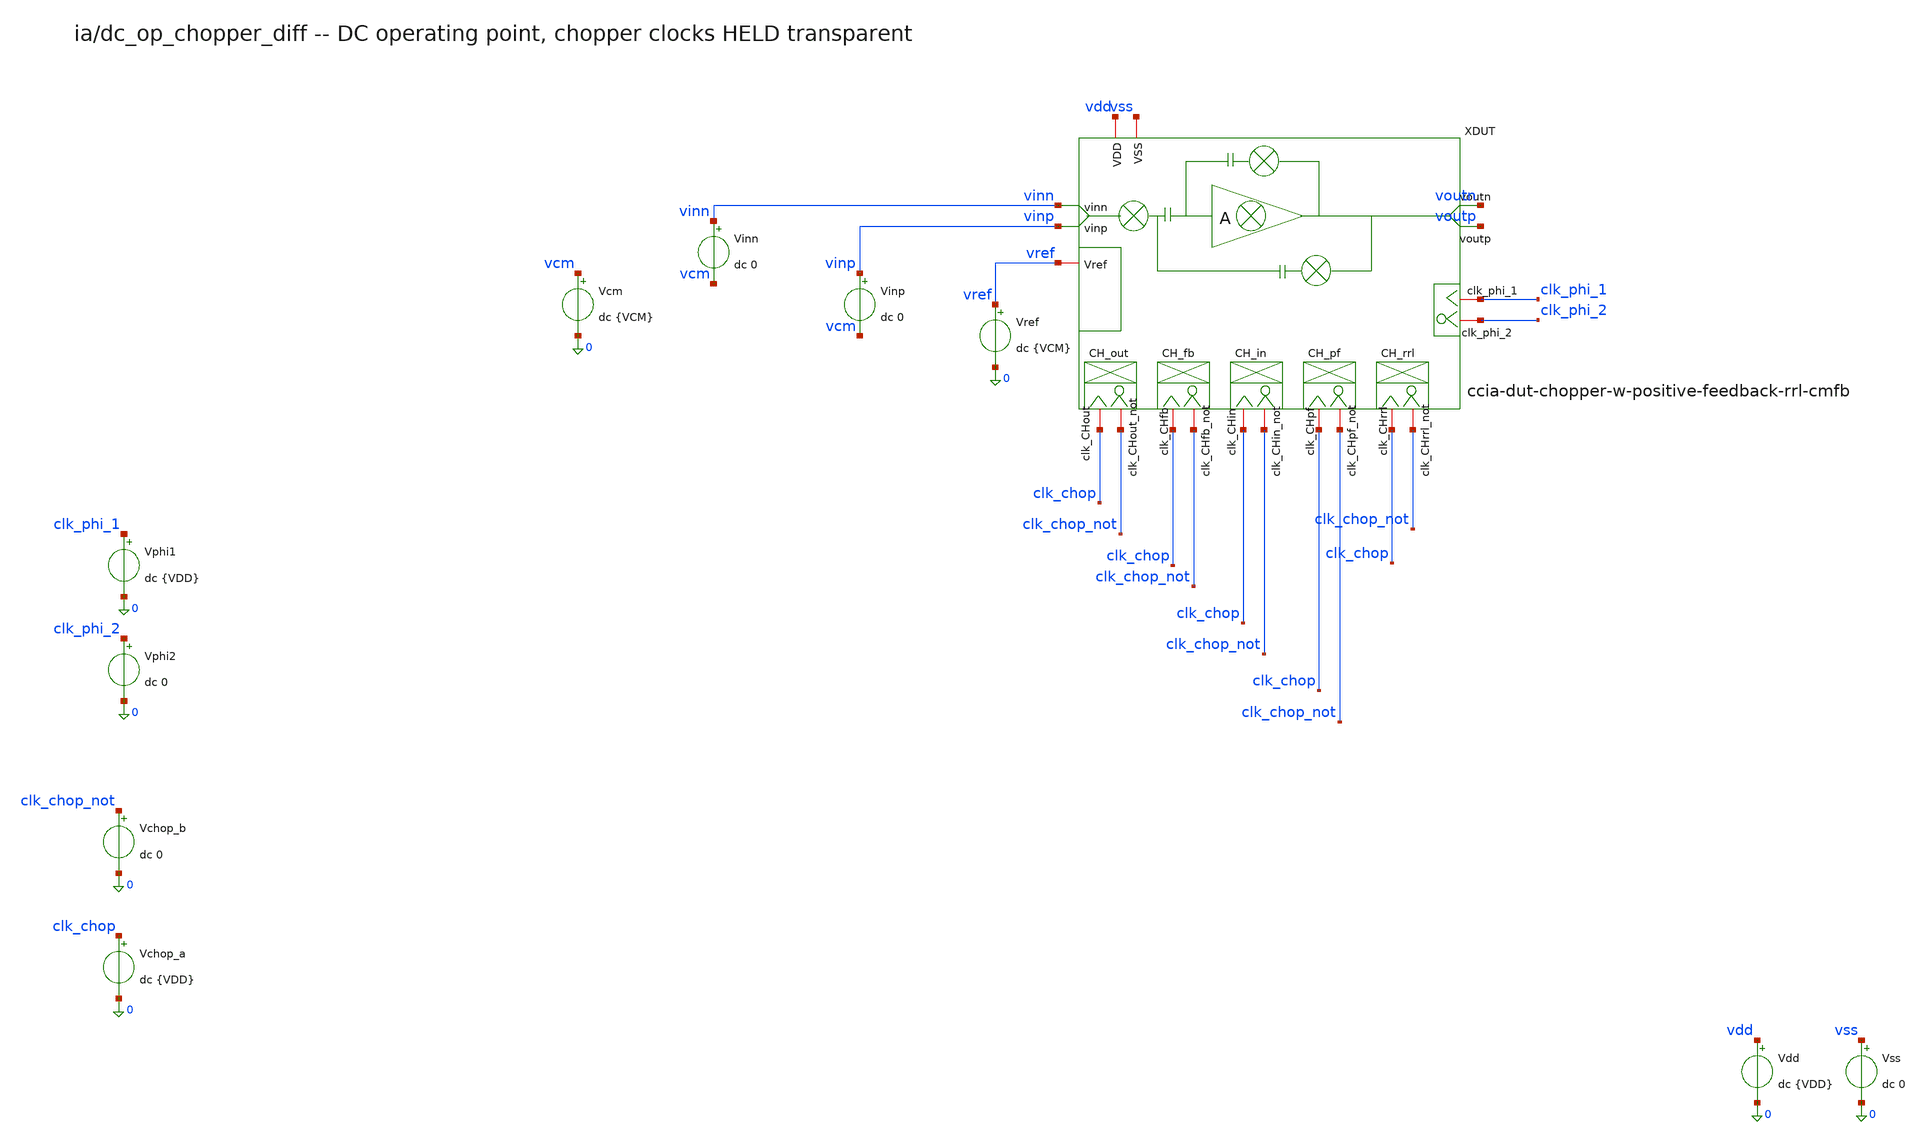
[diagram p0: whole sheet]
** sch_path: analog-db/drawings/ccia-02-QinwenFan-chopper-ripple-reduction/testbenches/ccia-dut/dc_op_chopper_diff_cmfb.sch
* Copyright 2026 MacAnalog Research Group
**.subckt dc_op_chopper_diff_cmfb
XDUT clk_chop clk_chop_not clk_chop clk_chop_not vref voutn vinn vinp voutp clk_chop clk_chop_not
+ vdd vss clk_chop clk_chop_not clk_chop clk_chop_not clk_phi_1 clk_phi_2
+ ccia-dut-chopper-w-positive-feedback-rrl-cmfb
Vdd vdd 0 dc {VDD}
Vss vss 0 dc 0
Vchop_a clk_chop 0 dc {VDD}
Vchop_b clk_chop_not 0 dc 0
Vphi1 clk_phi_1 0 dc {VDD}
Vphi2 clk_phi_2 0 dc 0
Vcm vcm 0 dc {VCM}
Vref vref 0 dc {VCM}
Vinp vinp vcm dc 0
Vinn vinn vcm dc 0
**** begin user architecture code


* TESTBENCH dc_op_chopper_diff_cmfb -- DUT ccia-dut-chopper-w-positive-feedback-rrl-cmfb
* produces: i_supply, vos, vocm
* recorded baseline: i_supply 219.4951 uA | vos 7.720941e-06 V | vocm 0.6096373 V (ia_004)
* bench bindings (circuits/ia_004_fan_chopper_rrl/analyses/)
.param VDD=1.2
.param VCM=0.6




* CCIA top level -- ccia-dut-chopper-w-positive-feedback-rrl.sch
* source: circuits/ia_004_fan_chopper_rrl/pdk/ihp-sg13g2/sizing.yaml
.param x_dut_cin1_main_value=16p  x_dut_cfb1_main_value=0.8p
.param x_dut_rb1_main_value=10Meg
* Cpf has no ia_004 knob (that composite drops the PF chopper); this drawing
* keeps it, so take ia_003_fan_chopper_pf's authored value.
.param x_dut_cpf1_main_value=0.8p
* --- behavioural-ideal CMFB servo --------------------------------------
* Built from primitives (Rm_p/Rm_n + E_cmfb) rather than
* shared/ideal/cmfb-output-ideal-amp-inv.sym, because that block's inner
* ideal-amp-fully-diff uses BARE param names (gm_val/rout_val) which the RRL
* instance already owns -- the servo gain could not be set independently.
*   vcm_ref   commanded output common mode
*   cmfb_rm   CM detector sense resistors (5Meg, not the 1Meg default: this core
*             is a true OTA with high Zout and the detector sits on voutp/voutn)
*   cmfb_gain servo gain A. Plant dvocm/dvb1 ~ 115 V/V, so A=10 gives loop gain
*             ~1150. A=100 SATURATES the servo and the output rails to 1.2 V
*             (measured) -- the amp_030 'stable spurious railed equilibrium'.
.param vcm_ref=0.6097
.param cmfb_rm=5Meg
* TUNED VIA ac_cm_reg (not via transient survival time). Valid points only --
* an AC sweep about a RAILED bias is meaningless, and A=30 rails (vocm 1.193):
*   A    Co     zcm_lf    peaking_db   dc vocm
*   30   any    ~2.98k    ~0.02        1.193  RAILED - numbers are garbage
*   10   10n    27.2      43.2         0.6097
*   10   1u     2.51k      7.05        0.6097
*   10   10u   14.83k      0.23        0.6097
*   3    1u     7.17k      2.42        0.6097  <- picked: passes <=6 dB, stiffest
*   3    10u   22.60k      0.00        0.6097  barely better than open loop
* Open loop (no CMFB) is zcm_lf 28.15k with 0.00 dB peaking.
.param cmfb_gain=3
* servo dominant pole f_p = 1/(2*pi*cmfb_ro*cmfb_co) ~ 16 Hz. Without a pole the
* VCVS is pure gain, the CM loop never rolls off and it oscillates (the clocked
* run died at 78 ns with vocm ringing 0.44<->0.78 V).
* Stability grid on a 200 us clocked run (A x cmfb_co):
*        160p     1n      10n
*   A=10  1.7e-5  3.2e-5  COMPLETES
*   A=3   1.3e-5  COMPLETES COMPLETES
*   A=1   7.0e-5  4.5e-5  COMPLETES
* A=10/10n picked: it completes AND keeps the most loop gain.
.param cmfb_ro=1Meg
.param cmfb_co=1u
.param vb1_main=0.5 vb2_main=0.75 vb3_main=0.45 vb4_main=0.55




* CCIA core opamp -- two-stage-opamp-core[-w-stage-breakout].sch
* (= circuits/amp_026_fan_chopper_ota, namespaced _MAIN in the composite)
.param x_dut_xm1_main_w=20u x_dut_xm1_main_l=1u
.param x_dut_xm2_main_w=20u x_dut_xm2_main_l=0.5u
.param x_dut_xm3_main_w=20u x_dut_xm3_main_l=0.5u
.param x_dut_xm4_main_w=4.7u x_dut_xm4_main_l=1u
.param x_dut_xm5_main_w=4.7u x_dut_xm5_main_l=1u
.param x_dut_xm6_main_w=10u x_dut_xm6_main_l=1u
.param x_dut_xm7_main_w=10u x_dut_xm7_main_l=1u
.param x_dut_xm8_main_w=6.2u x_dut_xm8_main_l=1u
.param x_dut_xm9_main_w=6.2u x_dut_xm9_main_l=1u
.param x_dut_xm10_main_w=10u x_dut_xm10_main_l=0.3u
.param x_dut_xm11_main_w=10u x_dut_xm11_main_l=0.3u
.param x_dut_xm12_main_w=5u x_dut_xm12_main_l=0.3u
.param x_dut_xm13_main_w=5u x_dut_xm13_main_l=0.3u
.param x_dut_xm14_main_w=6u x_dut_xm14_main_l=0.5u
.param x_dut_xm15_main_w=6u x_dut_xm15_main_l=0.5u
* Miller compensation cap
.param x_dut_cm1_main_value=1p




* RRL switched-capacitor network -- rrl-switched-capa-integrator.sch
* (= circuits/sup_003_rrl_sc_integrator, namespaced _RRL)
.param x_dut_cs1_rrl_value=1p  x_dut_caz1_rrl_value=1p  x_dut_cint1_rrl_value=4p
.param vb1_rrl=0.45 vb2_rrl=0.75 vb3_rrl=0.55 vcmfb_rrl=0.6
* behavioural compensation cell (shared/ideal/ideal-amp-fully-diff.sch).
* gm_val is ia_004's parent override (10u, not sup_003's own 100u): at the
* registry 5 kHz default the un-scaled Gm makes the discrete-time RRL loop
* gain > 1 and the clocked transient diverges.
.param gm_val=10u rout_val=10Meg cout_val=100f
.param rin_val=1T cin_val=10f




* RRL integrator opamp -- integrator-switchcap-opamp.sch
* (= circuits/amp_027_fan_rrl_ota, namespaced _OPAMP_RRL)
.param x_dut_xm1_opamp_rrl_w=20u x_dut_xm1_opamp_rrl_l=1u
.param x_dut_xm2_opamp_rrl_w=20u x_dut_xm2_opamp_rrl_l=0.5u
.param x_dut_xm3_opamp_rrl_w=20u x_dut_xm3_opamp_rrl_l=0.5u
.param x_dut_xm4_opamp_rrl_w=10u x_dut_xm4_opamp_rrl_l=1u
.param x_dut_xm5_opamp_rrl_w=4u x_dut_xm5_opamp_rrl_l=0.5u
.param x_dut_xm6_opamp_rrl_w=4u x_dut_xm6_opamp_rrl_l=0.5u
.param x_dut_xm7_opamp_rrl_w=4u x_dut_xm7_opamp_rrl_l=0.5u
.param x_dut_xm8_opamp_rrl_w=4u x_dut_xm8_opamp_rrl_l=0.5u
.param x_dut_xm9_opamp_rrl_w=10u x_dut_xm9_opamp_rrl_l=0.3u
.param x_dut_xm10_opamp_rrl_w=10u x_dut_xm10_opamp_rrl_l=0.3u
.param x_dut_xm11_opamp_rrl_w=5u x_dut_xm11_opamp_rrl_l=0.3u
.param x_dut_xm12_opamp_rrl_w=5u x_dut_xm12_opamp_rrl_l=0.3u
.param x_dut_xm13_opamp_rrl_w=6u x_dut_xm13_opamp_rrl_l=1u
.param x_dut_xm14_opamp_rrl_w=6u x_dut_xm14_opamp_rrl_l=1u
.param x_dut_xm15_opamp_rrl_w=2u x_dut_xm15_opamp_rrl_l=1u
.param x_dut_xm16_opamp_rrl_w=2u x_dut_xm16_opamp_rrl_l=1u




* Switches -- shared/transmission_gate_pair.sch, used by EVERY chopper
* (in/fb/out/pf/rrl) and by the RRL's SC switches.
* Held at the PDK geometry floor and deliberately NOT sized yet.
.param tg_n_w=0.18u tg_n_l=0.13u
.param tg_p_w=0.18u tg_p_l=0.13u




.control
  save all
  set filetype=binary
  op
  let i_supply = abs(i(Vdd))
  let vos = v(voutp) - v(voutn)
  let vocm = (v(voutp) + v(voutn))/2
  print i_supply vos vocm
  * op has a single data row, so there is nothing to graph - dump the bias
  * point instead. `show` is the interactive companion to these prints.
  print v(voutp) v(voutn) v(vinp) v(vinn) v(vref)
  write dc_op_chopper_diff_cmfb.raw
.endc




.lib cornerMOSlv.lib mos_tt
.lib cornerRES.lib res_typ
.lib cornerCAP.lib cap_typ
.temp 27


**** end user architecture code
**.ends
.end
